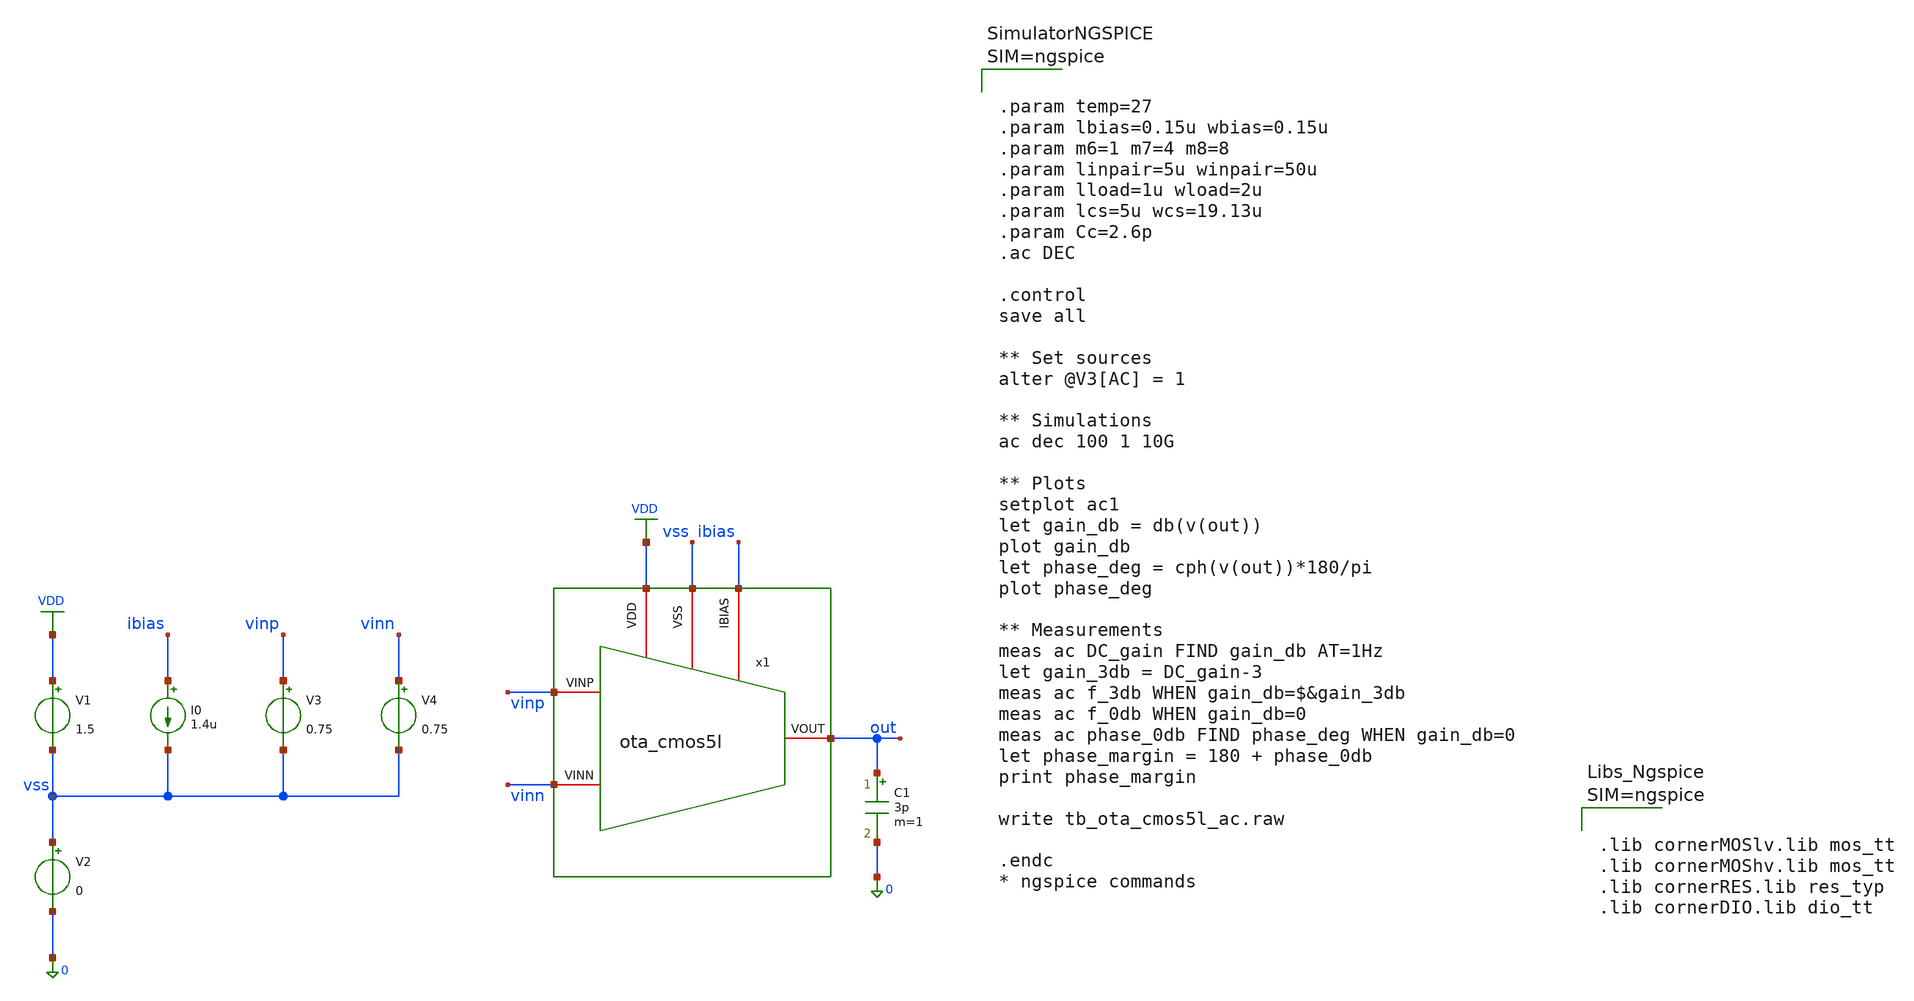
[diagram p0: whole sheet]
** sch_path: designs/libs/tb_analog/tb_ota_cmos5l_ac/tb_ota_cmos5l_ac.sch
**.subckt tb_ota_cmos5l_ac
x1 vss ibias VDD vinn vinp out ota_cmos5l
C1 out 0 3p m=1
I0 ibias vss 1.4u
V1 VDD vss 1.5
V2 vss 0 0
V3 vinp vss 0.75
V4 vinn vss 0.75
**** begin user architecture code



.param temp=27
.param lbias=0.15u wbias=0.15u
.param m6=1 m7=4 m8=8
.param linpair=5u winpair=50u
.param lload=1u wload=2u
.param lcs=5u wcs=19.13u
.param Cc=2.6p
.ac DEC

.control
save all

** Set sources
alter @V3[AC] = 1

** Simulations
ac dec 100 1 10G

** Plots
setplot ac1
let gain_db = db(v(out))
plot gain_db
let phase_deg = cph(v(out))*180/pi
plot phase_deg

** Measurements
meas ac DC_gain FIND gain_db AT=1Hz
let gain_3db = DC_gain-3
meas ac f_3db WHEN gain_db=$&gain_3db
meas ac f_0db WHEN gain_db=0
meas ac phase_0db FIND phase_deg WHEN gain_db=0
let phase_margin = 180 + phase_0db
print phase_margin

write tb_ota_cmos5l_ac.raw

.endc
* ngspice commands






.lib cornerMOSlv.lib mos_tt
.lib cornerMOShv.lib mos_tt
.lib cornerRES.lib res_typ
.lib cornerDIO.lib dio_tt



**** end user architecture code
**.ends

* expanding   symbol:
*+  /foss/designs/Programmable-Instrumentation-Amplifier-IP/designs/libs/core_analog/ota_cmos5l/ota_cmos5l.sym # of pins=6
** sym_path: /foss/designs/Programmable-Instrumentation-Amplifier-IP/designs/libs/core_analog/ota_cmos5l/ota_cmos5l.sym
** sch_path: /foss/designs/Programmable-Instrumentation-Amplifier-IP/designs/libs/core_analog/ota_cmos5l/ota_cmos5l.sch
.subckt ota_cmos5l VSS IBIAS VDD VINN VINP VOUT
*.iopin IBIAS
*.iopin VDD
*.iopin VSS
*.iopin VOUT
*.iopin VINP
*.iopin VINN
XM6 net1 net1 vdd vdd sg13_lv_pmos w={wbias} l={lbias} ng=1 m={m6} mm_ok=1
XM7 net5 net1 vdd vdd sg13_lv_pmos w={wbias} l={lbias} ng=1 m={m7} mm_ok=1
XM8 net6 net1 vdd vdd sg13_lv_pmos w={wbias} l={lbias} ng=1 m={m8} mm_ok=1
XM1 net7 VINN net2 vdd sg13_lv_pmos w={winpair} l={linpair} ng=1 m=1 mm_ok=1
XM2 net8 VINP net2 vdd sg13_lv_pmos w={winpair} l={linpair} ng=1 m=1 mm_ok=1
XM3 net3 net3 gnd gnd sg13_lv_nmos w={wload} l={lload} ng=1 m=1 mm_ok=1
XM4 net4 net3 gnd gnd sg13_lv_nmos w={wload} l={lload} ng=1 m=1 mm_ok=1
XM5 net9 net4 gnd gnd sg13_lv_nmos w={wcs} l={lcs} ng=1 m=1 mm_ok=1
C1 net10 net9 {Cc} m=1
XR1 net4 net10 sub! rhigh w=0.5e-6 l=1.95e-6 m=1 b=0 mm_ok=1
**** begin user architecture code



.include ota_cmos5l.save
.param temp=27
.param lbias=0.15u wbias=0.15u
.param m6=1 m7=4 m8=10
.param linpair=3u winpair=20u
.param lload=0.5u wload=0.42u
.param lcs=5u wcs=19.13u
.param Cc=1.5p
.control
op
write ota_cmos5l.raw
.endc



**** end user architecture code
**** begin user architecture code



.lib cornerMOSlv.lib mos_tt
.lib cornerMOShv.lib mos_tt
.lib cornerRES.lib res_typ
.lib cornerDIO.lib dio_tt



**** end user architecture code
VIBIAS net1 ibias 0
.save i(vibias)
VID7 net5 net2 0
.save i(vid7)
VID8 net6 VOUT 0
.save i(vid8)
VIVDD VDD vdd 0
.save i(vivdd)
.save v(vinp)
.save v(vinn)
.save v(vout)
VID1 net7 net3 0
.save i(vid1)
VID2 net8 net4 0
.save i(vid2)
VID5 VOUT net9 0
.save i(vid5)
.ends

.GLOBAL VDD
.end
